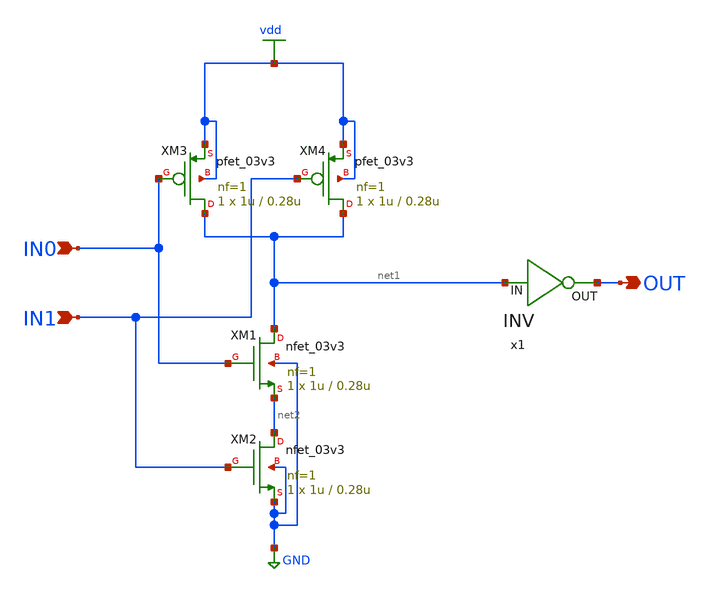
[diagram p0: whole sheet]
** sch_path: AND/AND.sch
**.subckt AND OUT IN0 IN1
*.opin OUT
*.ipin IN0
*.ipin IN1
XM1 net1 IN0 net2 GND nfet_03v3 L=0.28u W=1u nf=1 ad='int((nf+1)/2) * W/nf * 0.18u' as='int((nf+2)/2) * W/nf * 0.18u'
+ pd='2*int((nf+1)/2) * (W/nf + 0.18u)' ps='2*int((nf+2)/2) * (W/nf + 0.18u)' nrd='0.18u / W' nrs='0.18u / W'
+ sa=0 sb=0 sd=0 m=1
XM2 net2 IN1 GND GND nfet_03v3 L=0.28u W=1u nf=1 ad='int((nf+1)/2) * W/nf * 0.18u' as='int((nf+2)/2) * W/nf * 0.18u'
+ pd='2*int((nf+1)/2) * (W/nf + 0.18u)' ps='2*int((nf+2)/2) * (W/nf + 0.18u)' nrd='0.18u / W' nrs='0.18u / W'
+ sa=0 sb=0 sd=0 m=1
XM3 net1 IN0 vdd vdd pfet_03v3 L=0.28u W=1u nf=1 ad='int((nf+1)/2) * W/nf * 0.18u' as='int((nf+2)/2) * W/nf * 0.18u'
+ pd='2*int((nf+1)/2) * (W/nf + 0.18u)' ps='2*int((nf+2)/2) * (W/nf + 0.18u)' nrd='0.18u / W' nrs='0.18u / W'
+ sa=0 sb=0 sd=0 m=1
XM4 net1 IN1 vdd vdd pfet_03v3 L=0.28u W=1u nf=1 ad='int((nf+1)/2) * W/nf * 0.18u' as='int((nf+2)/2) * W/nf * 0.18u'
+ pd='2*int((nf+1)/2) * (W/nf + 0.18u)' ps='2*int((nf+2)/2) * (W/nf + 0.18u)' nrd='0.18u / W' nrs='0.18u / W'
+ sa=0 sb=0 sd=0 m=1
x1 OUT net1 INV
**.ends

* expanding   symbol:  AND/INV.sym # of pins=2
** sym_path: AND/INV.sym
** sch_path: AND/INV.sch
.subckt INV OUT IN
*.ipin IN
*.opin OUT
XM1 OUT IN VDD VDD pfet_03v3 L=0.28u W=1u nf=1 ad='int((nf+1)/2) * W/nf * 0.18u' as='int((nf+2)/2) * W/nf * 0.18u'
+ pd='2*int((nf+1)/2) * (W/nf + 0.18u)' ps='2*int((nf+2)/2) * (W/nf + 0.18u)' nrd='0.18u / W' nrs='0.18u / W'
+ sa=0 sb=0 sd=0 m=1
XM2 OUT IN GND GND nfet_03v3 L=0.28u W=0.5u nf=1 ad='int((nf+1)/2) * W/nf * 0.18u' as='int((nf+2)/2) * W/nf * 0.18u'
+ pd='2*int((nf+1)/2) * (W/nf + 0.18u)' ps='2*int((nf+2)/2) * (W/nf + 0.18u)' nrd='0.18u / W' nrs='0.18u / W'
+ sa=0 sb=0 sd=0 m=1
.ends

.GLOBAL GND
.GLOBAL vdd
.GLOBAL VDD
.end
